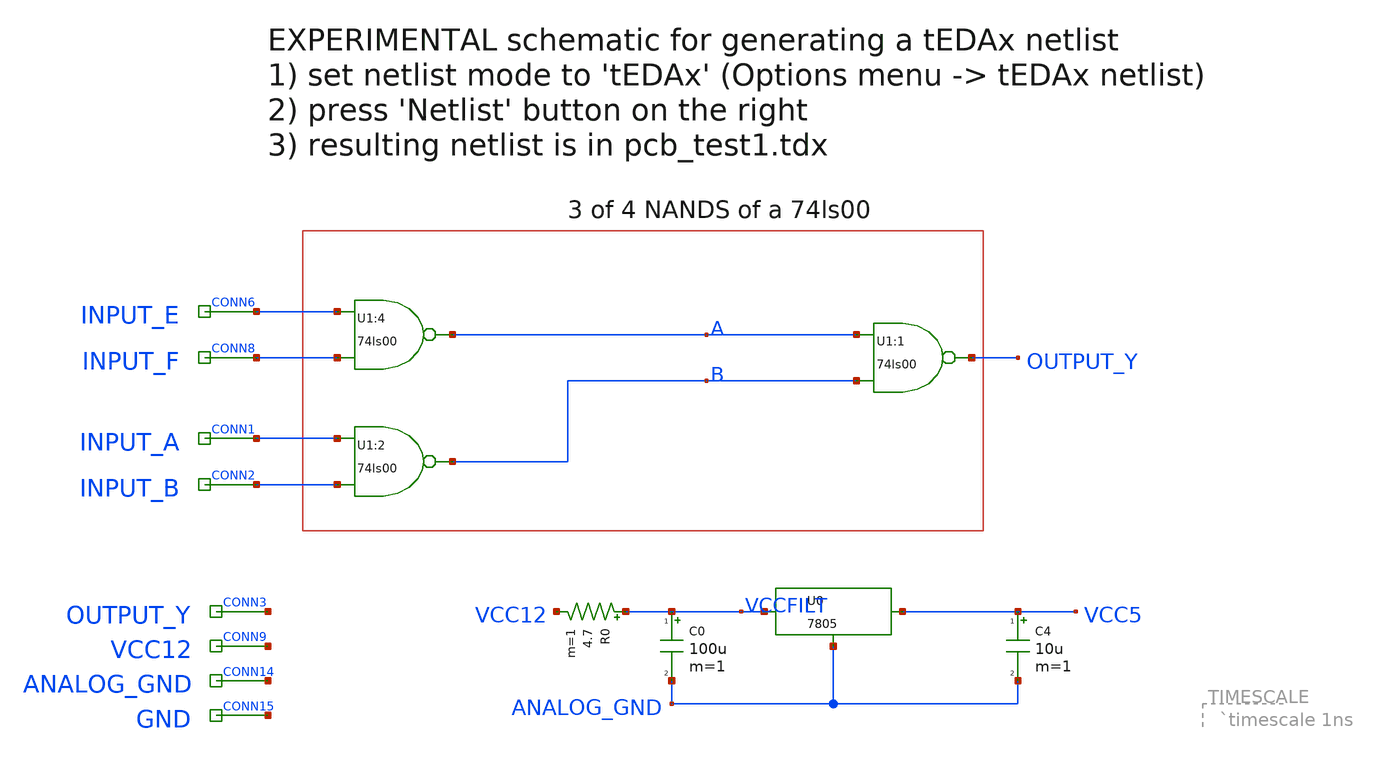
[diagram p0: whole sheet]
** sch_path: library/pcb/pcb_test1.sch
**.subckt pcb_test1 INPUT_A INPUT_B OUTPUT_Y INPUT_E INPUT_F VCC12 ANALOG_GND GND
*.ipin INPUT_A
*.ipin INPUT_B
*.ipin OUTPUT_Y
*.ipin INPUT_E
*.ipin INPUT_F
*.ipin VCC12
*.ipin ANALOG_GND
*.ipin GND
C0 VCCFILT ANALOG_GND 100u m=1
xU0 VCCFILT ANALOG_GND VCC5 r7805
C4 VCC5 ANALOG_GND 10u m=1
R0 VCCFILT VCC12 4.7 m=1
**** begin user architecture code

initial begin
  $dumpfile("dumpfile.vcd");
  $dumpvars;
  INPUT_E=0;
  INPUT_F=0;
  INPUT_A=0;
  INPUT_B=0;
  ANALOG_GND=0;
  #10000;
  INPUT_A=1;
  INPUT_B=1;
  #10000;
  INPUT_E=1;
  INPUT_F=1;
  #10000;
  INPUT_F=0;
  #10000;
  INPUT_B=0;
  #10000;
  $finish;
end

assign VCC12=1;



**** end user architecture code
**.ends
.end
